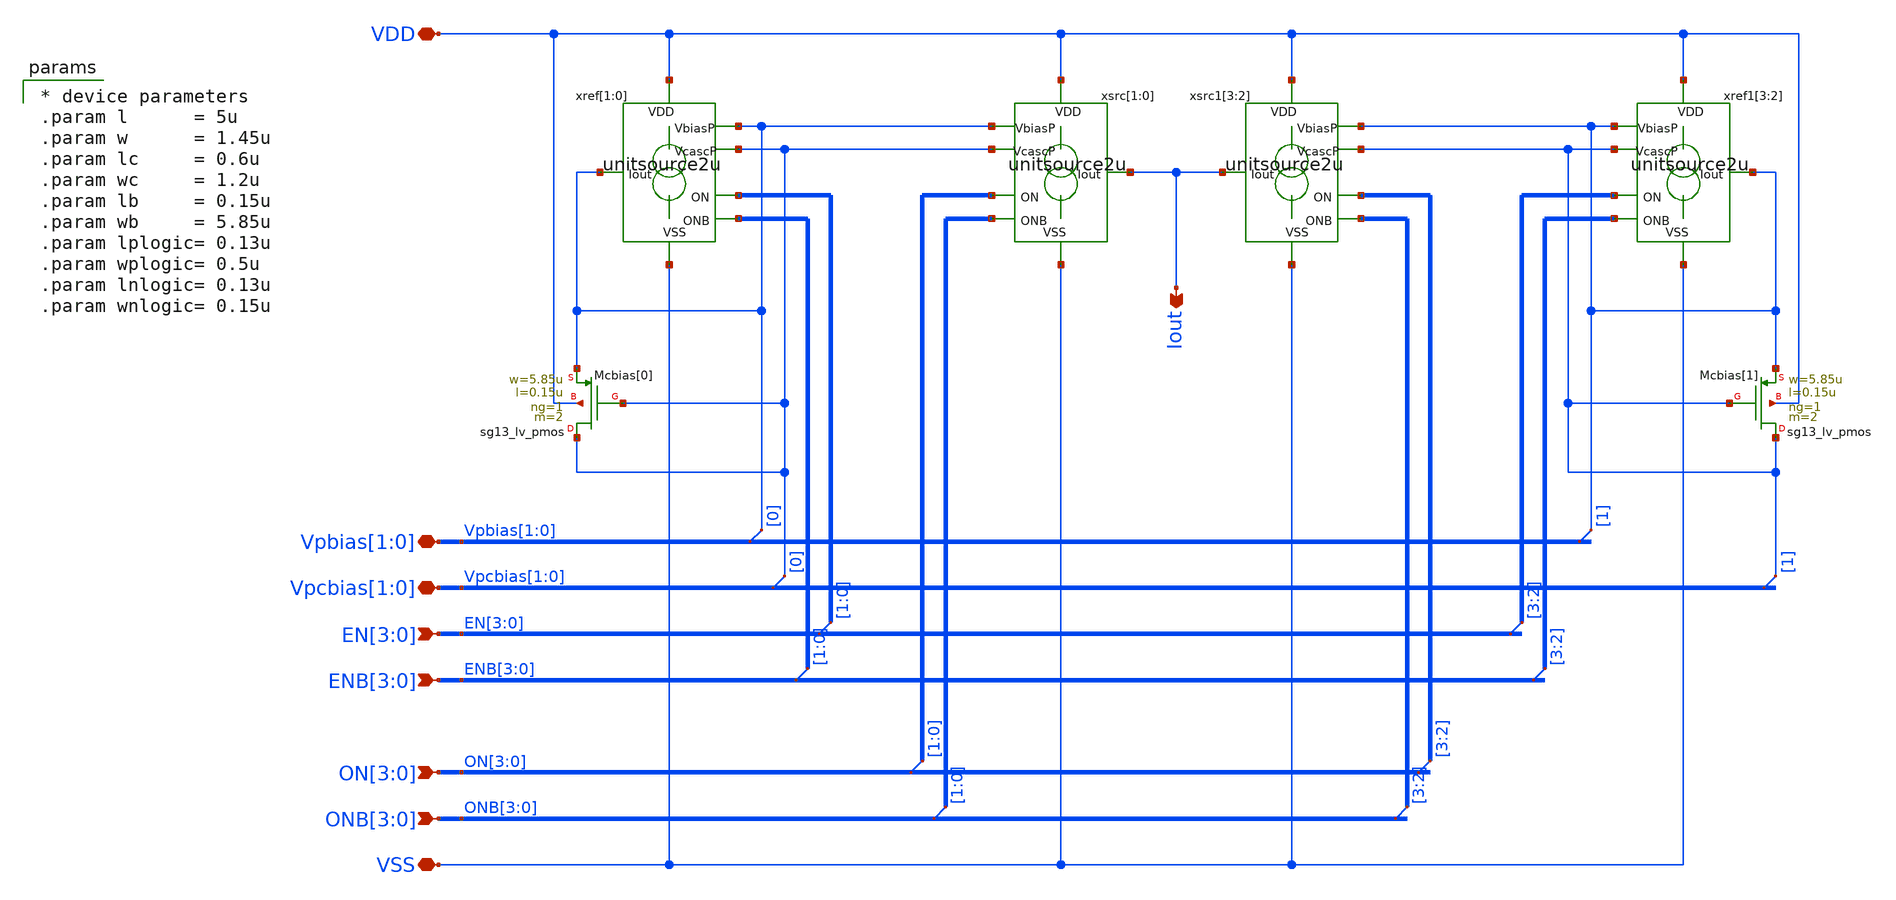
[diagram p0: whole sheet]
** sch_path: xschem/dac4module.sch
**.subckt dac4module Iout ON[3],ON[2],ON[1],ON[0] ONB[3],ONB[2],ONB[1],ONB[0] VSS VDD
*+ Vpcbias[1],Vpcbias[0] EN[3],EN[2],EN[1],EN[0] ENB[3],ENB[2],ENB[1],ENB[0] Vpbias[1],Vpbias[0]
*.opin Iout
*.ipin ON[3],ON[2],ON[1],ON[0]
*.ipin ONB[3],ONB[2],ONB[1],ONB[0]
*.iopin VSS
*.iopin VDD
*.iopin Vpcbias[1],Vpcbias[0]
*.ipin EN[3],EN[2],EN[1],EN[0]
*.ipin ENB[3],ENB[2],ENB[1],ENB[0]
*.iopin Vpbias[1],Vpbias[0]
XMcbias[0] Vpcbias[0] Vpcbias[0] Vpbias[0] VDD sg13_lv_pmos w=5.85u l=0.15u ng=1 m=2 mm_ok=1
xref[1] VDD Vpbias[0] EN[1] ENB[1] Vpbias[0] Vpcbias[0] VSS unitsource2u
xref[0] VDD Vpbias[0] EN[0] ENB[0] Vpbias[0] Vpcbias[0] VSS unitsource2u
xsrc[1] VDD Vpbias[0] ON[1] ONB[1] Iout Vpcbias[0] VSS unitsource2u
xsrc[0] VDD Vpbias[0] ON[0] ONB[0] Iout Vpcbias[0] VSS unitsource2u
XMcbias[1] Vpcbias[1] Vpcbias[1] Vpbias[1] VDD sg13_lv_pmos w=5.85u l=0.15u ng=1 m=2 mm_ok=1
xref1[3] VDD Vpbias[1] EN[3] ENB[3] Vpbias[1] Vpcbias[1] VSS unitsource2u
xref1[2] VDD Vpbias[1] EN[2] ENB[2] Vpbias[1] Vpcbias[1] VSS unitsource2u
xsrc1[3] VDD Vpbias[1] ON[3] ONB[3] Iout Vpcbias[1] VSS unitsource2u
xsrc1[2] VDD Vpbias[1] ON[2] ONB[2] Iout Vpcbias[1] VSS unitsource2u
* tap: EN[3:0] --> EN[1:0]
* tap: ENB[3:0] --> ENB[1:0]
* tap: ENB[3:0] --> ENB[3:2]
* tap: EN[3:0] --> EN[3:2]
* tap: ON[3:0] --> ON[1:0]
* tap: ONB[3:0] --> ONB[1:0]
* tap: ON[3:0] --> ON[3:2]
* tap: ONB[3:0] --> ONB[3:2]
* tap: Vpbias[1:0] --> Vpbias[0]
* tap: Vpcbias[1:0] --> Vpcbias[0]
* tap: Vpbias[1:0] --> Vpbias[1]
* tap: Vpcbias[1:0] --> Vpcbias[1]
**** begin user architecture code

* device parameters
.param l      = 5u
.param w      = 1.45u
.param lc     = 0.6u
.param wc     = 1.2u
.param lb     = 0.15u
.param wb     = 5.85u
.param lplogic= 0.13u
.param wplogic= 0.5u
.param lnlogic= 0.13u
.param wnlogic= 0.15u


**** end user architecture code
**.ends

* expanding   symbol:  unitsource2u.sym # of pins=7
** sym_path: xschem/unitsource2u.sym
** sch_path: xschem/unitsource2u.sch
.subckt unitsource2u VDD VbiasP ON ONB Iout VcascP VSS
*.iopin VSS
*.iopin VDD
*.iopin VbiasP
*.iopin VcascP
*.ipin ON
*.ipin ONB
*.iopin Iout
xnonoverlap VDD VSS ON ONB on_n off_n nonoverlap
xsw VDD off_n Vcasc on_n VcascP cascodeswitch_pmos
xsrc VDD VbiasP Vcasc Iout pcsource2u
.ends


* expanding   symbol:  nonoverlap.sym # of pins=6
** sym_path: xschem/nonoverlap.sym
** sch_path: xschem/nonoverlap.sch
.subckt nonoverlap VDD VSS INP INN OUTN OUTP
*.iopin VSS
*.iopin VDD
*.ipin INP
*.ipin INN
*.opin OUTP
*.opin OUTN
XM1 OUTN INP VDD VDD sg13_lv_pmos w=0.3u l=0.13u ng=1 m=1 mm_ok=1
XM2 OUTP INN VDD VDD sg13_lv_pmos w=0.3u l=0.13u ng=1 m=1 mm_ok=1
XM3 OUTN OUTP VSS VSS sg13_lv_nmos w=0.15u l=0.52u ng=1 m=1 mm_ok=1
XM4 OUTP OUTN VSS VSS sg13_lv_nmos w=0.15u l=0.52u ng=1 m=1 mm_ok=1
.ends


* expanding   symbol:  cascodeswitch_pmos.sym # of pins=5
** sym_path: xschem/cascodeswitch_pmos.sym
** sch_path: xschem/cascodeswitch_pmos.sch
.subckt cascodeswitch_pmos VDD off_n Vcasc on_n Vbpcasc
*.ipin off_n
*.ipin Vbpcasc
*.opin Vcasc
*.ipin on_n
*.ipin VDD
XMpullup Vcasc off_n VDD VDD sg13_lv_pmos w=0.3u l=0.13u ng=1 m=1 mm_ok=1
XMbias Vbpcasc on_n Vcasc VDD sg13_lv_pmos w=0.3u l=0.13u ng=1 m=1 mm_ok=1
.ends


* expanding   symbol:  pcsource2u.sym # of pins=4
** sym_path: xschem/pcsource2u.sym
** sch_path: xschem/pcsource2u.sch
.subckt pcsource2u VDD VbiasP VcascodeP Iout
*.ipin VcascodeP
*.ipin VbiasP
*.opin Iout
*.ipin VDD
XMsrc drain net4 VDD net1 sg13_lv_pmos w=1.45u l=5u ng=1 m=1 mm_ok=1
XMcasc Iout net3 drain net2 sg13_lv_pmos w=1.2u l=0.6u ng=1 m=1 mm_ok=1
Vgsrc net4 VbiasP 0
.save i(vgsrc)
Vgcasc net3 VcascodeP 0
.save i(vgcasc)
Vbsrc VDD net1 0
.save i(vbsrc)
Vbcasc VDD net2 0
.save i(vbcasc)
.ends

.end
